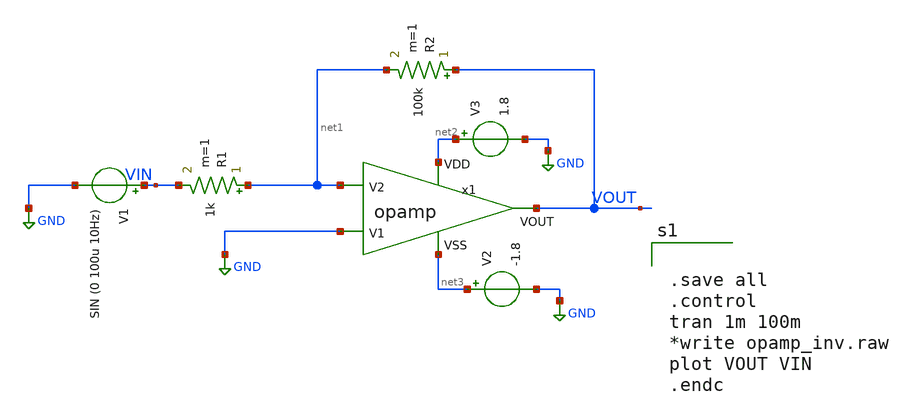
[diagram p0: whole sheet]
** sch_path: opamp_inv.sch
**.subckt opamp_inv
V1 VIN GND SIN (0 100u 10Hz)
V2 net3 GND -1.8
V3 net2 GND 1.8
R1 net1 VIN 1k m=1
R2 VOUT net1 100k m=1
x1 net2 net3 GND net1 VOUT opamp
**** begin user architecture code


.save all
.control
tran 1m 100m
*write opamp_inv.raw
plot VOUT VIN
.endc



** opencircuitdesign pdks install
.lib $::SKYWATER_MODELS/sky130.lib.spice tt


**** end user architecture code
**.ends

* expanding   symbol:  /foss/designs/chipalooza2024/sky130_hcmus_ip__instramp/opamp.sym # of pins=5
** sym_path: xschem/opamp.sym
** sch_path: xschem/opamp.sch
.subckt opamp VDD VSS V1 V2 VOUT
*.ipin VSS
*.ipin VDD
*.ipin V2
*.ipin V1
*.opin VOUT
XM2 net4 V2 net1 VSS sky130_fd_pr__nfet_g5v0d10v5 L=1 W=18 nf=1 ad='int((nf+1)/2) * W/nf * 0.29' as='int((nf+2)/2) * W/nf * 0.29'
+ pd='2*int((nf+1)/2) * (W/nf + 0.29)' ps='2*int((nf+2)/2) * (W/nf + 0.29)' nrd='0.29 / W' nrs='0.29 / W'
+ sa=0 sb=0 sd=0 mult=1 m=1
XM1 net5 net4 VDD VDD sky130_fd_pr__pfet_g5v0d10v5 L=1 W=30 nf=1 ad='int((nf+1)/2) * W/nf * 0.29' as='int((nf+2)/2) * W/nf * 0.29'
+ pd='2*int((nf+1)/2) * (W/nf + 0.29)' ps='2*int((nf+2)/2) * (W/nf + 0.29)' nrd='0.29 / W' nrs='0.29 / W'
+ sa=0 sb=0 sd=0 mult=1 m=1
XM4 net5 V1 net1 VSS sky130_fd_pr__nfet_g5v0d10v5 L=1 W=18 nf=1 ad='int((nf+1)/2) * W/nf * 0.29' as='int((nf+2)/2) * W/nf * 0.29'
+ pd='2*int((nf+1)/2) * (W/nf + 0.29)' ps='2*int((nf+2)/2) * (W/nf + 0.29)' nrd='0.29 / W' nrs='0.29 / W'
+ sa=0 sb=0 sd=0 mult=1 m=1
XM5 net1 net6 VSS VSS sky130_fd_pr__nfet_g5v0d10v5 L=1 W=15.171 nf=1 ad='int((nf+1)/2) * W/nf * 0.29'
+ as='int((nf+2)/2) * W/nf * 0.29' pd='2*int((nf+1)/2) * (W/nf + 0.29)' ps='2*int((nf+2)/2) * (W/nf + 0.29)'
+ nrd='0.29 / W' nrs='0.29 / W' sa=0 sb=0 sd=0 mult=1 m=1
XM6 VOUT net6 VSS VSS sky130_fd_pr__nfet_g5v0d10v5 L=1 W=19 nf=1 ad='int((nf+1)/2) * W/nf * 0.29' as='int((nf+2)/2) * W/nf * 0.29'
+ pd='2*int((nf+1)/2) * (W/nf + 0.29)' ps='2*int((nf+2)/2) * (W/nf + 0.29)' nrd='0.29 / W' nrs='0.29 / W'
+ sa=0 sb=0 sd=0 mult=1 m=1
XM7 net6 net6 VSS VSS sky130_fd_pr__nfet_g5v0d10v5 L=1 W=20 nf=1 ad='int((nf+1)/2) * W/nf * 0.29' as='int((nf+2)/2) * W/nf * 0.29'
+ pd='2*int((nf+1)/2) * (W/nf + 0.29)' ps='2*int((nf+2)/2) * (W/nf + 0.29)' nrd='0.29 / W' nrs='0.29 / W'
+ sa=0 sb=0 sd=0 mult=1 m=1
XM3 net4 net4 VDD VDD sky130_fd_pr__pfet_g5v0d10v5 L=1 W=30 nf=1 ad='int((nf+1)/2) * W/nf * 0.29' as='int((nf+2)/2) * W/nf * 0.29'
+ pd='2*int((nf+1)/2) * (W/nf + 0.29)' ps='2*int((nf+2)/2) * (W/nf + 0.29)' nrd='0.29 / W' nrs='0.29 / W'
+ sa=0 sb=0 sd=0 mult=1 m=1
XM8 VOUT net5 VDD VDD sky130_fd_pr__pfet_g5v0d10v5 L=1 W=38 nf=1 ad='int((nf+1)/2) * W/nf * 0.29' as='int((nf+2)/2) * W/nf * 0.29'
+ pd='2*int((nf+1)/2) * (W/nf + 0.29)' ps='2*int((nf+2)/2) * (W/nf + 0.29)' nrd='0.29 / W' nrs='0.29 / W'
+ sa=0 sb=0 sd=0 mult=2 m=2
XC1 net7 net5 sky130_fd_pr__cap_mim_m3_1 W=5.5 L=10 MF=10 m=10
V_ibias net8 net6 0
.save i(v_ibias)
XR5 net2 VDD VSS sky130_fd_pr__res_high_po_0p69 L=18.58 mult=1 m=1
XR1 net3 net2 VSS sky130_fd_pr__res_high_po_0p69 L=18.58 mult=1 m=1
XR2 net8 net3 VSS sky130_fd_pr__res_high_po_0p69 L=18.58 mult=1 m=1
XR3 net7 VOUT VSS sky130_fd_pr__res_high_po_0p69 L=2.41 mult=1 m=1
.ends

.GLOBAL GND
.end
